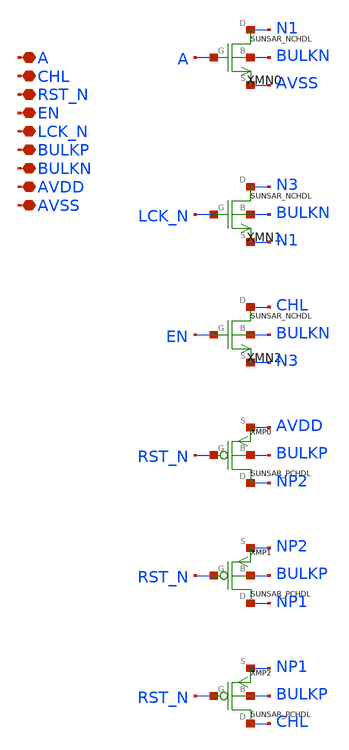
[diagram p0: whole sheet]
** sch_path: ip/sun_sar9b_sky130nm/design/SUN_SAR9B_SKY130NM/SUNSAR_SARLTX1_CV.sch
**.subckt SUNSAR_SARLTX1_CV A CHL RST_N EN LCK_N BULKP BULKN AVDD AVSS
*.iopin A
*.iopin CHL
*.iopin RST_N
*.iopin EN
*.iopin LCK_N
*.iopin BULKP
*.iopin BULKN
*.iopin AVDD
*.iopin AVSS
XMN0 N1 A AVSS BULKN SUNSAR_NCHDL
XMN1 N3 LCK_N N1 BULKN SUNSAR_NCHDL
XMN2 CHL EN N3 BULKN SUNSAR_NCHDL
XMP0 NP2 RST_N AVDD BULKP SUNSAR_PCHDL
XMP1 NP1 RST_N NP2 BULKP SUNSAR_PCHDL
XMP2 CHL RST_N NP1 BULKP SUNSAR_PCHDL
**.ends
.end
